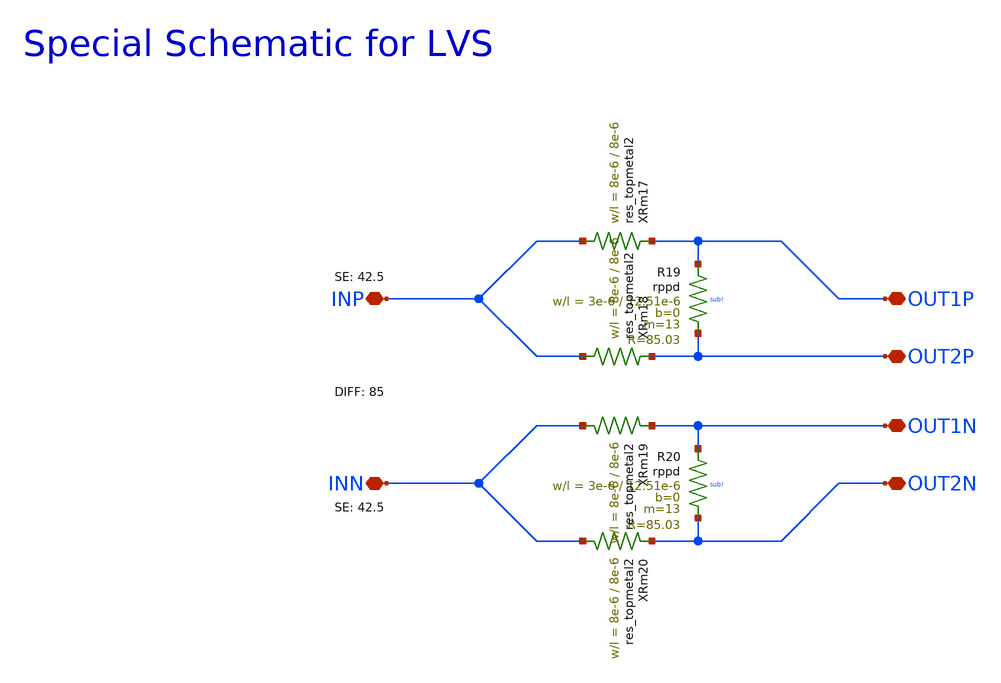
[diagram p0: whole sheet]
** sch_path: mWATTBAT/design_data/lvs/WILKINSON_LVS.sch
**.subckt WILKINSON_LVS INP INN OUT1P OUT2N OUT1N OUT2P
*.iopin INP
*.iopin INN
*.iopin OUT1P
*.iopin OUT2N
*.iopin OUT1N
*.iopin OUT2P
XR19 OUT1P OUT2P sub! rppd w=3e-6 l=12.51e-6 m=13 b=0 mm_ok=1
XR20 OUT1N OUT2N sub! rppd w=3e-6 l=12.51e-6 m=13 b=0 mm_ok=1
XRm17 INP OUT1P res_topmetal2 w=8e-6 l=8e-6
XRm18 INP OUT2P res_topmetal2 w=8e-6 l=8e-6
XRm19 INN OUT1N res_topmetal2 w=8e-6 l=8e-6
XRm20 INN OUT2N res_topmetal2 w=8e-6 l=8e-6
**.ends
.end
